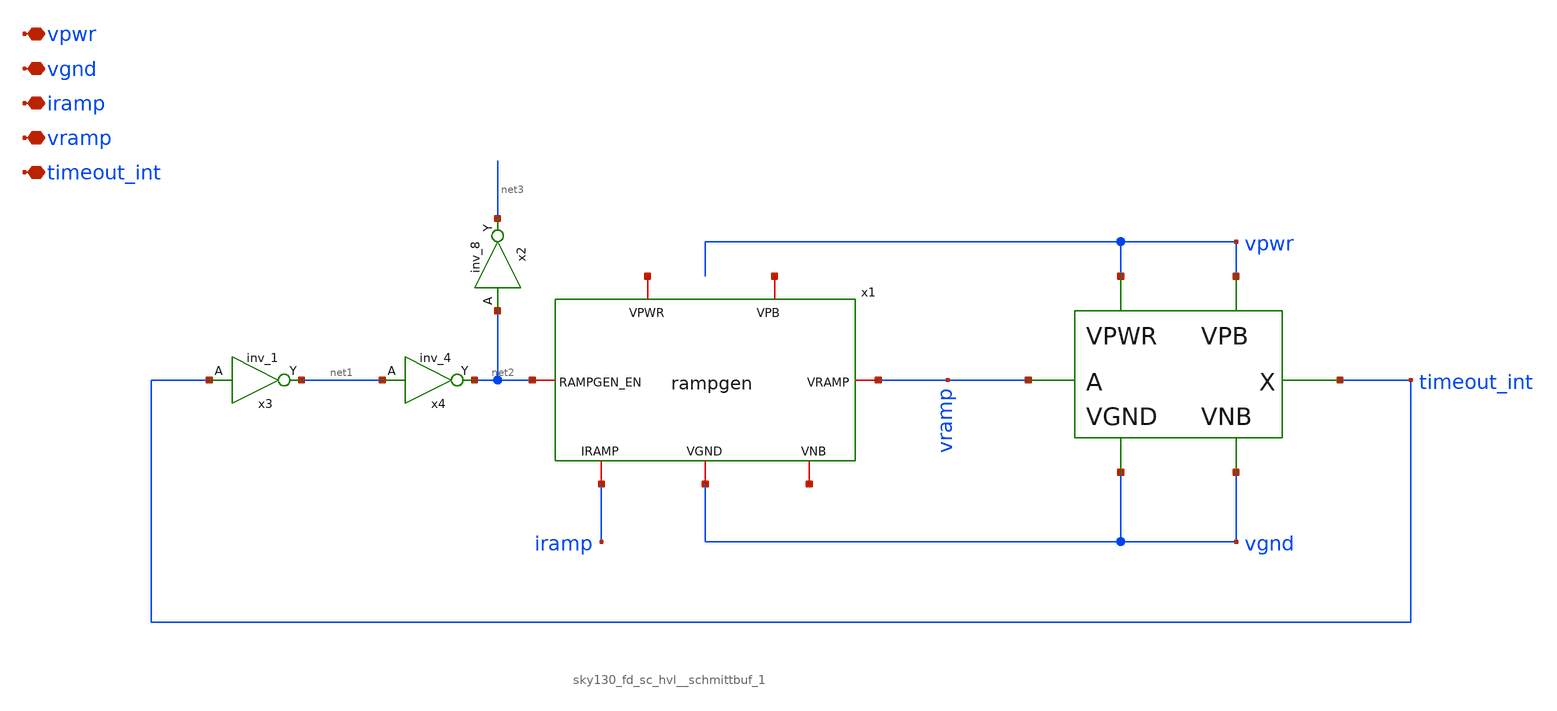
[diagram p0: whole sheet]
** sch_path: design/oscillator/oscillator.sch
**.subckt oscillator vpwr vgnd iramp vramp timeout_int
*.iopin vpwr
*.iopin vgnd
*.iopin iramp
*.iopin vramp
*.iopin timeout_int
x1 net4 vgnd net5 net6 iramp vramp net2 rampgen
x3 timeout_int VGND VNB VPB VPWR net1 sky130_fd_sc_hvl__inv_1
x4 net1 VGND VNB VPB VPWR net2 sky130_fd_sc_hvl__inv_4
x5 vramp vgnd vgnd vpwr vpwr timeout_int sky130_fd_sc_hvl__schmittbuf_1
x2 net2 VGND VNB VPB VPWR net3 sky130_fd_sc_hvl__inv_8
**.ends

* expanding   symbol:  design/oscillator/rampgen.sym # of pins=7
** sym_path: design/oscillator/rampgen.sym
** sch_path: design/oscillator/rampgen.sch
.subckt rampgen VPWR VGND VPB VNB IRAMP VRAMP RAMPGEN_EN
*.iopin VPWR
*.iopin VGND
*.iopin VPB
*.iopin VNB
*.iopin IRAMP
*.iopin VRAMP
*.iopin RAMPGEN_EN
XM1 IRAMP IRAMP VGND VNB sky130_fd_pr__nfet_g5v0d10v5 L=1 W=5 nf=1 ad='int((nf+1)/2) * W/nf * 0.29' as='int((nf+2)/2) * W/nf * 0.29'
+ pd='2*int((nf+1)/2) * (W/nf + 0.29)' ps='2*int((nf+2)/2) * (W/nf + 0.29)' nrd='0.29 / W' nrs='0.29 / W'
+ sa=0 sb=0 sd=0 mult=1 m=1
XM2 net3 IRAMP VGND VNB sky130_fd_pr__nfet_g5v0d10v5 L=1 W=5 nf=1 ad='int((nf+1)/2) * W/nf * 0.29' as='int((nf+2)/2) * W/nf * 0.29'
+ pd='2*int((nf+1)/2) * (W/nf + 0.29)' ps='2*int((nf+2)/2) * (W/nf + 0.29)' nrd='0.29 / W' nrs='0.29 / W'
+ sa=0 sb=0 sd=0 mult=1 m=1
XM3 net2 IRAMP VGND VNB sky130_fd_pr__nfet_g5v0d10v5 L=1 W=5 nf=1 ad='int((nf+1)/2) * W/nf * 0.29' as='int((nf+2)/2) * W/nf * 0.29'
+ pd='2*int((nf+1)/2) * (W/nf + 0.29)' ps='2*int((nf+2)/2) * (W/nf + 0.29)' nrd='0.29 / W' nrs='0.29 / W'
+ sa=0 sb=0 sd=0 mult=15 m=15
XM4 VRAMP RAMPGEN_EN net2 VNB sky130_fd_pr__nfet_g5v0d10v5 L=1 W=5 nf=1 ad='int((nf+1)/2) * W/nf * 0.29'
+ as='int((nf+2)/2) * W/nf * 0.29' pd='2*int((nf+1)/2) * (W/nf + 0.29)' ps='2*int((nf+2)/2) * (W/nf + 0.29)'
+ nrd='0.29 / W' nrs='0.29 / W' sa=0 sb=0 sd=0 mult=15 m=15
XM5 net3 net3 VPWR VPB sky130_fd_pr__pfet_g5v0d10v5 L=1 W=5 nf=1 ad='int((nf+1)/2) * W/nf * 0.29' as='int((nf+2)/2) * W/nf * 0.29'
+ pd='2*int((nf+1)/2) * (W/nf + 0.29)' ps='2*int((nf+2)/2) * (W/nf + 0.29)' nrd='0.29 / W' nrs='0.29 / W'
+ sa=0 sb=0 sd=0 mult=1 m=1
XM6 VRAMP RAMPGEN_EN net1 VPB sky130_fd_pr__pfet_g5v0d10v5 L=1 W=5 nf=1 ad='int((nf+1)/2) * W/nf * 0.29'
+ as='int((nf+2)/2) * W/nf * 0.29' pd='2*int((nf+1)/2) * (W/nf + 0.29)' ps='2*int((nf+2)/2) * (W/nf + 0.29)'
+ nrd='0.29 / W' nrs='0.29 / W' sa=0 sb=0 sd=0 mult=1 m=1
XM7 net1 net3 VPWR VPB sky130_fd_pr__pfet_g5v0d10v5 L=1 W=5 nf=1 ad='int((nf+1)/2) * W/nf * 0.29' as='int((nf+2)/2) * W/nf * 0.29'
+ pd='2*int((nf+1)/2) * (W/nf + 0.29)' ps='2*int((nf+2)/2) * (W/nf + 0.29)' nrd='0.29 / W' nrs='0.29 / W'
+ sa=0 sb=0 sd=0 mult=1 m=1
XC1 VRAMP VGND sky130_fd_pr__cap_mim_m3_1 W=20 L=26 MF=1 m=1
.ends

.end
